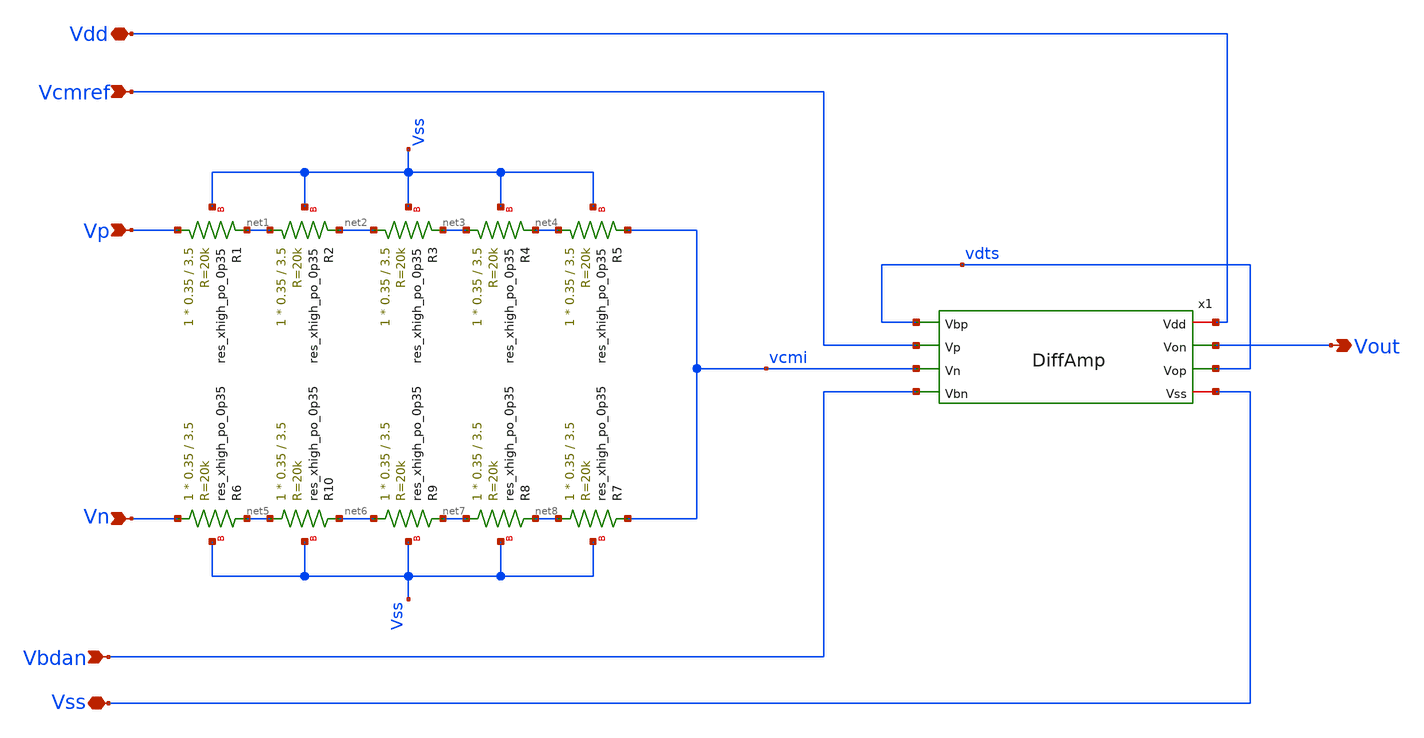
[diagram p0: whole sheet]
** sch_path: Circuits/Examples/OpAmp/CMMFeedback.sch
**.subckt CMMFeedback Vbdan Vout Vp Vcmref Vn Vss Vdd
*.ipin Vbdan
*.opin Vout
*.ipin Vp
*.ipin Vcmref
*.ipin Vn
*.iopin Vss
*.iopin Vdd
XR1 Vp net1 Vss sky130_fd_pr__res_xhigh_po_0p35 L=3.5 mult=1 m=1
XR2 net1 net2 Vss sky130_fd_pr__res_xhigh_po_0p35 L=3.5 mult=1 m=1
XR3 net2 net3 Vss sky130_fd_pr__res_xhigh_po_0p35 L=3.5 mult=1 m=1
XR4 net3 net4 Vss sky130_fd_pr__res_xhigh_po_0p35 L=3.5 mult=1 m=1
XR5 net4 vcmi Vss sky130_fd_pr__res_xhigh_po_0p35 L=3.5 mult=1 m=1
XR6 Vn net5 Vss sky130_fd_pr__res_xhigh_po_0p35 L=3.5 mult=1 m=1
XR10 net5 net6 Vss sky130_fd_pr__res_xhigh_po_0p35 L=3.5 mult=1 m=1
XR9 net6 net7 Vss sky130_fd_pr__res_xhigh_po_0p35 L=3.5 mult=1 m=1
XR8 net7 net8 Vss sky130_fd_pr__res_xhigh_po_0p35 L=3.5 mult=1 m=1
XR7 net8 vcmi Vss sky130_fd_pr__res_xhigh_po_0p35 L=3.5 mult=1 m=1
x1 Vdd vdts Vout vdts Vcmref vcmi Vbdan Vss DiffAmp
**.ends

* expanding   symbol:  /home/jakob/Documents/RALF/Circuits/Examples/OpAmp/DiffAmp.sym # of pins=8
** sym_path: Circuits/Examples/OpAmp/DiffAmp.sym
** sch_path: Circuits/Examples/OpAmp/DiffAmp.sch
.subckt DiffAmp Vdd Vbp Von Vop Vp Vn Vbn Vss
*.iopin Vdd
*.iopin Vss
*.ipin Vp
*.ipin Vn
*.ipin Vbn
*.ipin Vbp
*.opin Vop
*.opin Von
XM1 Vop Vp vmid Vss sky130_fd_pr__nfet_01v8 L=1 W=1 nf=1 ad='int((nf+1)/2) * W/nf * 0.29' as='int((nf+2)/2) * W/nf * 0.29'
+ pd='2*int((nf+1)/2) * (W/nf + 0.29)' ps='2*int((nf+2)/2) * (W/nf + 0.29)' nrd='0.29 / W' nrs='0.29 / W'
+ sa=0 sb=0 sd=0 mult=1 m=1
XM2 Von Vn vmid Vss sky130_fd_pr__nfet_01v8 L=1 W=1 nf=1 ad='int((nf+1)/2) * W/nf * 0.29' as='int((nf+2)/2) * W/nf * 0.29'
+ pd='2*int((nf+1)/2) * (W/nf + 0.29)' ps='2*int((nf+2)/2) * (W/nf + 0.29)' nrd='0.29 / W' nrs='0.29 / W'
+ sa=0 sb=0 sd=0 mult=1 m=1
XM3 Vop Vbp Vdd Vdd sky130_fd_pr__pfet_01v8 L=1 W=2 nf=1 ad='int((nf+1)/2) * W/nf * 0.29' as='int((nf+2)/2) * W/nf * 0.29'
+ pd='2*int((nf+1)/2) * (W/nf + 0.29)' ps='2*int((nf+2)/2) * (W/nf + 0.29)' nrd='0.29 / W' nrs='0.29 / W'
+ sa=0 sb=0 sd=0 mult=1 m=1
XM4 Von Vbp Vdd Vdd sky130_fd_pr__pfet_01v8 L=1 W=2 nf=1 ad='int((nf+1)/2) * W/nf * 0.29' as='int((nf+2)/2) * W/nf * 0.29'
+ pd='2*int((nf+1)/2) * (W/nf + 0.29)' ps='2*int((nf+2)/2) * (W/nf + 0.29)' nrd='0.29 / W' nrs='0.29 / W'
+ sa=0 sb=0 sd=0 mult=1 m=1
XM5 vmid Vbn Vss Vss sky130_fd_pr__nfet_01v8 L=2 W=1 nf=1 ad='int((nf+1)/2) * W/nf * 0.29' as='int((nf+2)/2) * W/nf * 0.29'
+ pd='2*int((nf+1)/2) * (W/nf + 0.29)' ps='2*int((nf+2)/2) * (W/nf + 0.29)' nrd='0.29 / W' nrs='0.29 / W'
+ sa=0 sb=0 sd=0 mult=1 m=1
.ends

.end
